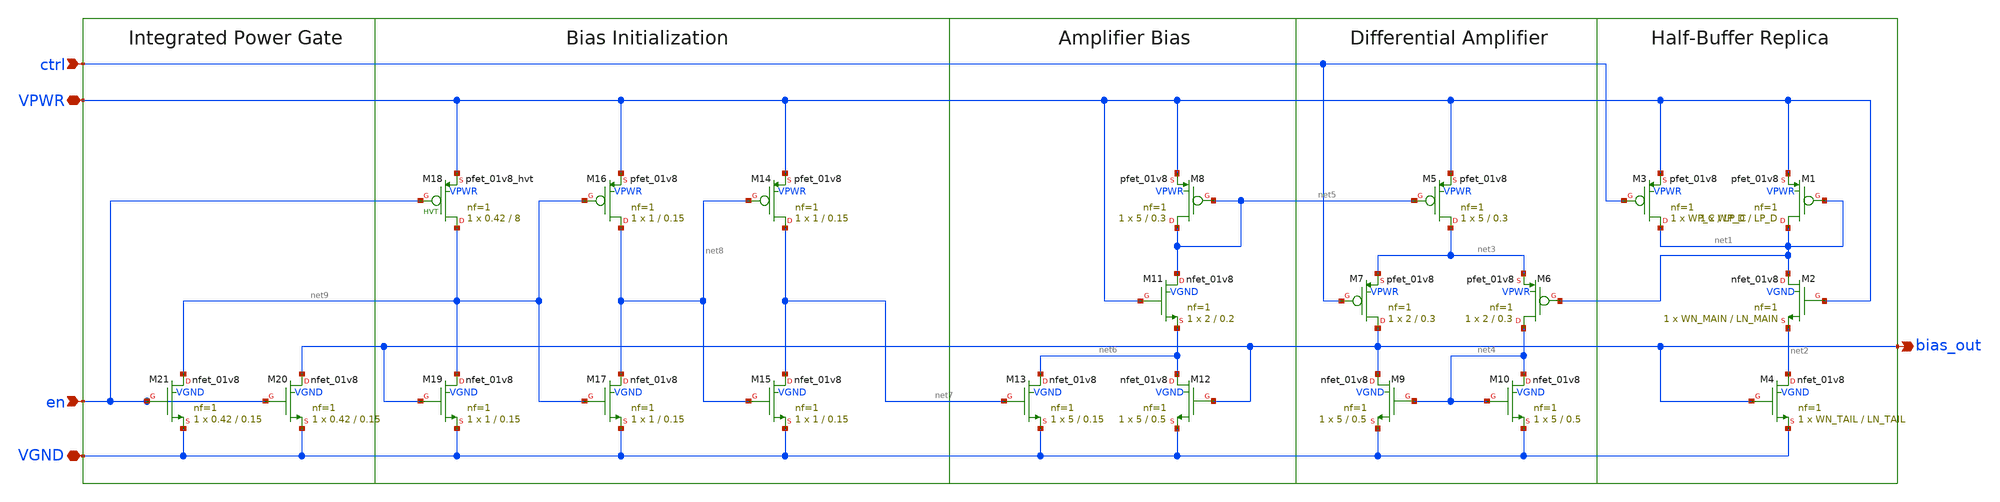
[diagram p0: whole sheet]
** sch_path: simple_vco/v1/bias_gen.sch
**.subckt bias_gen VPWR VGND en ctrl bias_out
*.iopin VPWR
*.iopin VGND
*.ipin en
*.ipin ctrl
*.opin bias_out
XM8 net5 net5 VPWR VPWR sky130_fd_pr__pfet_01v8 L=0.3 W=5 nf=1 ad='int((1 + 1)/2) * 5 / 1 * 0.29' as='int((1 + 2)/2) * 5 / 1 * 0.29'
+ pd='2*int((1 + 1)/2) * (5 / 1 + 0.29)' ps='2*int((1 + 2)/2) * (5 / 1 + 0.29)' nrd='0.29 / 5 ' nrs='0.29 / 5 '
+ sa=0 sb=0 sd=0 mult=1 m=1
XM7 bias_out ctrl net3 VPWR sky130_fd_pr__pfet_01v8 L=0.3 W=2 nf=1 ad='int((1 + 1)/2) * 2 / 1 * 0.29'
+ as='int((1 + 2)/2) * 2 / 1 * 0.29' pd='2*int((1 + 1)/2) * (2 / 1 + 0.29)' ps='2*int((1 + 2)/2) * (2 / 1 + 0.29)'
+ nrd='0.29 / 2 ' nrs='0.29 / 2 ' sa=0 sb=0 sd=0 mult=1 m=1
XM6 net4 net1 net3 VPWR sky130_fd_pr__pfet_01v8 L=0.3 W=2 nf=1 ad='int((1 + 1)/2) * 2 / 1 * 0.29' as='int((1 + 2)/2) * 2 / 1 * 0.29'
+ pd='2*int((1 + 1)/2) * (2 / 1 + 0.29)' ps='2*int((1 + 2)/2) * (2 / 1 + 0.29)' nrd='0.29 / 2 ' nrs='0.29 / 2 '
+ sa=0 sb=0 sd=0 mult=1 m=1
XM3 net1 ctrl VPWR VPWR sky130_fd_pr__pfet_01v8 L=LP_C W=WP_C nf=1 ad='int((1 + 1)/2) * WP_C / 1 * 0.29'
+ as='int((1 + 2)/2) * WP_C / 1 * 0.29' pd='2*int((1 + 1)/2) * (WP_C / 1 + 0.29)' ps='2*int((1 + 2)/2) * (WP_C / 1 + 0.29)'
+ nrd='0.29 / WP_C ' nrs='0.29 / WP_C ' sa=0 sb=0 sd=0 mult=1 m=1
XM1 net1 net1 VPWR VPWR sky130_fd_pr__pfet_01v8 L=LP_D W=WP_D nf=1 ad='int((1 + 1)/2) * WP_D / 1 * 0.29'
+ as='int((1 + 2)/2) * WP_D / 1 * 0.29' pd='2*int((1 + 1)/2) * (WP_D / 1 + 0.29)' ps='2*int((1 + 2)/2) * (WP_D / 1 + 0.29)'
+ nrd='0.29 / WP_D ' nrs='0.29 / WP_D ' sa=0 sb=0 sd=0 mult=1 m=1
XM5 net3 net5 VPWR VPWR sky130_fd_pr__pfet_01v8 L=0.3 W=5 nf=1 ad='int((1 + 1)/2) * 5 / 1 * 0.29' as='int((1 + 2)/2) * 5 / 1 * 0.29'
+ pd='2*int((1 + 1)/2) * (5 / 1 + 0.29)' ps='2*int((1 + 2)/2) * (5 / 1 + 0.29)' nrd='0.29 / 5 ' nrs='0.29 / 5 '
+ sa=0 sb=0 sd=0 mult=1 m=1
XM9 bias_out net4 VGND VGND sky130_fd_pr__nfet_01v8 L=0.5 W=5 nf=1 ad='int((1 + 1)/2) * 5 / 1 * 0.29'
+ as='int((1 + 2)/2) * 5 / 1 * 0.29' pd='2*int((1 + 1)/2) * (5 / 1 + 0.29)' ps='2*int((1 + 2)/2) * (5 / 1 + 0.29)'
+ nrd='0.29 / 5 ' nrs='0.29 / 5 ' sa=0 sb=0 sd=0 mult=1 m=1
XM10 net4 net4 VGND VGND sky130_fd_pr__nfet_01v8 L=0.5 W=5 nf=1 ad='int((1 + 1)/2) * 5 / 1 * 0.29' as='int((1 + 2)/2) * 5 / 1 * 0.29'
+ pd='2*int((1 + 1)/2) * (5 / 1 + 0.29)' ps='2*int((1 + 2)/2) * (5 / 1 + 0.29)' nrd='0.29 / 5 ' nrs='0.29 / 5 '
+ sa=0 sb=0 sd=0 mult=1 m=1
XM11 net5 VPWR net6 VGND sky130_fd_pr__nfet_01v8 L=0.2 W=2 nf=1 ad='int((1 + 1)/2) * 2 / 1 * 0.29' as='int((1 + 2)/2) * 2 / 1 * 0.29'
+ pd='2*int((1 + 1)/2) * (2 / 1 + 0.29)' ps='2*int((1 + 2)/2) * (2 / 1 + 0.29)' nrd='0.29 / 2 ' nrs='0.29 / 2 '
+ sa=0 sb=0 sd=0 mult=1 m=1
XM12 net6 bias_out VGND VGND sky130_fd_pr__nfet_01v8 L=0.5 W=5 nf=1 ad='int((1 + 1)/2) * 5 / 1 * 0.29'
+ as='int((1 + 2)/2) * 5 / 1 * 0.29' pd='2*int((1 + 1)/2) * (5 / 1 + 0.29)' ps='2*int((1 + 2)/2) * (5 / 1 + 0.29)'
+ nrd='0.29 / 5 ' nrs='0.29 / 5 ' sa=0 sb=0 sd=0 mult=1 m=1
XM13 net6 net7 VGND VGND sky130_fd_pr__nfet_01v8 L=0.15 W=5 nf=1 ad='int((1 + 1)/2) * 5 / 1 * 0.29' as='int((1 + 2)/2) * 5 / 1 * 0.29'
+ pd='2*int((1 + 1)/2) * (5 / 1 + 0.29)' ps='2*int((1 + 2)/2) * (5 / 1 + 0.29)' nrd='0.29 / 5 ' nrs='0.29 / 5 '
+ sa=0 sb=0 sd=0 mult=1 m=1
XM14 net7 net8 VPWR VPWR sky130_fd_pr__pfet_01v8 L=0.15 W=1 nf=1 ad='int((1 + 1)/2) * 1 / 1 * 0.29' as='int((1 + 2)/2) * 1 / 1 * 0.29'
+ pd='2*int((1 + 1)/2) * (1 / 1 + 0.29)' ps='2*int((1 + 2)/2) * (1 / 1 + 0.29)' nrd='0.29 / 1 ' nrs='0.29 / 1 '
+ sa=0 sb=0 sd=0 mult=1 m=1
XM15 net7 net8 VGND VGND sky130_fd_pr__nfet_01v8 L=0.15 W=1 nf=1 ad='int((1 + 1)/2) * 1 / 1 * 0.29' as='int((1 + 2)/2) * 1 / 1 * 0.29'
+ pd='2*int((1 + 1)/2) * (1 / 1 + 0.29)' ps='2*int((1 + 2)/2) * (1 / 1 + 0.29)' nrd='0.29 / 1 ' nrs='0.29 / 1 '
+ sa=0 sb=0 sd=0 mult=1 m=1
XM16 net8 net9 VPWR VPWR sky130_fd_pr__pfet_01v8 L=0.15 W=1 nf=1 ad='int((1 + 1)/2) * 1 / 1 * 0.29' as='int((1 + 2)/2) * 1 / 1 * 0.29'
+ pd='2*int((1 + 1)/2) * (1 / 1 + 0.29)' ps='2*int((1 + 2)/2) * (1 / 1 + 0.29)' nrd='0.29 / 1 ' nrs='0.29 / 1 '
+ sa=0 sb=0 sd=0 mult=1 m=1
XM17 net8 net9 VGND VGND sky130_fd_pr__nfet_01v8 L=0.15 W=1 nf=1 ad='int((1 + 1)/2) * 1 / 1 * 0.29' as='int((1 + 2)/2) * 1 / 1 * 0.29'
+ pd='2*int((1 + 1)/2) * (1 / 1 + 0.29)' ps='2*int((1 + 2)/2) * (1 / 1 + 0.29)' nrd='0.29 / 1 ' nrs='0.29 / 1 '
+ sa=0 sb=0 sd=0 mult=1 m=1
XM19 net9 bias_out VGND VGND sky130_fd_pr__nfet_01v8 L=0.15 W=1 nf=1 ad='int((1 + 1)/2) * 1 / 1 * 0.29'
+ as='int((1 + 2)/2) * 1 / 1 * 0.29' pd='2*int((1 + 1)/2) * (1 / 1 + 0.29)' ps='2*int((1 + 2)/2) * (1 / 1 + 0.29)'
+ nrd='0.29 / 1 ' nrs='0.29 / 1 ' sa=0 sb=0 sd=0 mult=1 m=1
XM18 net9 en VPWR VPWR sky130_fd_pr__pfet_01v8_hvt L=8 W=0.42 nf=1 ad='int((1 + 1)/2) * 0.42 / 1 * 0.29'
+ as='int((1 + 2)/2) * 0.42 / 1 * 0.29' pd='2*int((1 + 1)/2) * (0.42 / 1 + 0.29)' ps='2*int((1 + 2)/2) * (0.42 / 1 + 0.29)'
+ nrd='0.29 / 0.42 ' nrs='0.29 / 0.42 ' sa=0 sb=0 sd=0 mult=1 m=1
XM20 bias_out en VGND VGND sky130_fd_pr__nfet_01v8 L=0.15 W=0.42 nf=1 ad='int((1 + 1)/2) * 0.42 / 1 * 0.29'
+ as='int((1 + 2)/2) * 0.42 / 1 * 0.29' pd='2*int((1 + 1)/2) * (0.42 / 1 + 0.29)' ps='2*int((1 + 2)/2) * (0.42 / 1 + 0.29)'
+ nrd='0.29 / 0.42 ' nrs='0.29 / 0.42 ' sa=0 sb=0 sd=0 mult=1 m=1
XM21 net9 en VGND VGND sky130_fd_pr__nfet_01v8 L=0.15 W=0.42 nf=1 ad='int((1 + 1)/2) * 0.42 / 1 * 0.29'
+ as='int((1 + 2)/2) * 0.42 / 1 * 0.29' pd='2*int((1 + 1)/2) * (0.42 / 1 + 0.29)' ps='2*int((1 + 2)/2) * (0.42 / 1 + 0.29)'
+ nrd='0.29 / 0.42 ' nrs='0.29 / 0.42 ' sa=0 sb=0 sd=0 mult=1 m=1
XM4 net2 bias_out VGND VGND sky130_fd_pr__nfet_01v8 L=LN_TAIL W=WN_TAIL nf=1 ad='int((1 + 1)/2) * WN_TAIL / 1 * 0.29'
+ as='int((1 + 2)/2) * WN_TAIL / 1 * 0.29' pd='2*int((1 + 1)/2) * (WN_TAIL / 1 + 0.29)' ps='2*int((1 + 2)/2) * (WN_TAIL / 1 + 0.29)'
+ nrd='0.29 / WN_TAIL ' nrs='0.29 / WN_TAIL ' sa=0 sb=0 sd=0 mult=1 m=1
XM2 net1 VPWR net2 VGND sky130_fd_pr__nfet_01v8 L=LN_MAIN W=WN_MAIN nf=1 ad='int((1 + 1)/2) * WN_MAIN / 1 * 0.29'
+ as='int((1 + 2)/2) * WN_MAIN / 1 * 0.29' pd='2*int((1 + 1)/2) * (WN_MAIN / 1 + 0.29)' ps='2*int((1 + 2)/2) * (WN_MAIN / 1 + 0.29)'
+ nrd='0.29 / WN_MAIN ' nrs='0.29 / WN_MAIN ' sa=0 sb=0 sd=0 mult=1 m=1
**.ends
.end
